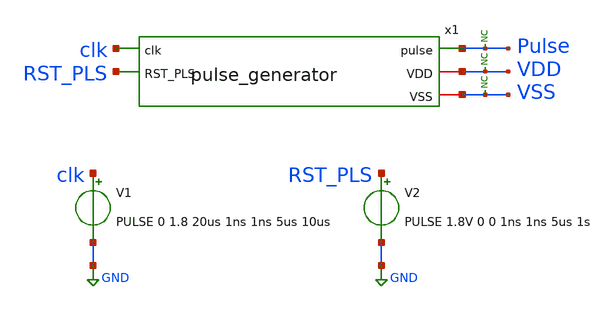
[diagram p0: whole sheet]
** sch_path: xschem/tests/pulse_generator/pulse_generator_test.sch
**.subckt pulse_generator_test
V1 clk GND PULSE 0 1.8 20us 1ns 1ns 5us 10us
V2 RST_PLS GND PULSE 1.8V 0 0 1ns 1ns 5us 1s
x1 clk Pulse VDD VSS RST_PLS pulse_generator
* noconn Pulse
* noconn VDD
* noconn VSS
**** begin user architecture code
 .lib $::SKYWATER_MODELS/sky130.lib.spice tt
.include $::SKYWATER_STDCELLS/sky130_fd_sc_hd.spice



.options acct list
.temp 25
vvcc VDD 0 dc 1.8
vvss VSS 0 0
.control
tran 0.1u 400u
* plot a b+2 clk+4 reset_b+6 x+8 y+10 q+12 qlatch+14
* plot RST_PLS-2 clk clk2+2 clk4+4 clk8+6 clk16+8 clk32+10 clk64+12 delayed+14 pulse+16
plot RST_PLS clk+2 Pulse+4
write pulse_generator_test.raw
.endc


**** end user architecture code
**.ends

* expanding   symbol:  pulse_generator.sym # of pins=5
** sym_path: xschem/src/pulse_generator/pulse_generator.sym
** sch_path: xschem/src/pulse_generator/pulse_generator.sch
.subckt pulse_generator clk pulse VDD VSS RST_PLS
*.ipin clk
*.ipin RST_PLS
*.opin pulse
*.iopin VDD
*.iopin VSS
x1 clk net1 RST_PLS VSS VSS VDD VDD clk2 net1 sky130_fd_sc_hd__dfrbp_1
x2 clk2 net2 RST_PLS VSS VSS VDD VDD clk4 net2 sky130_fd_sc_hd__dfrbp_1
x3 clk4 net3 RST_PLS VSS VSS VDD VDD clk8 net3 sky130_fd_sc_hd__dfrbp_1
x4 clk8 net4 RST_PLS VSS VSS VDD VDD clk16 net4 sky130_fd_sc_hd__dfrbp_1
x5 delayed clk64 VSS VSS VDD VDD pulse sky130_fd_sc_hd__xor2_1
* noconn pulse
x6 clk clk64 RST_PLS VSS VSS VDD VDD delayed net7 sky130_fd_sc_hd__dfrbp_1
* noconn #net7
x9 clk16 net5 RST_PLS VSS VSS VDD VDD clk32 net5 sky130_fd_sc_hd__dfrbp_1
x10 clk32 net6 RST_PLS VSS VSS VDD VDD clk64 net6 sky130_fd_sc_hd__dfrbp_1
.ends

.GLOBAL GND
.end
